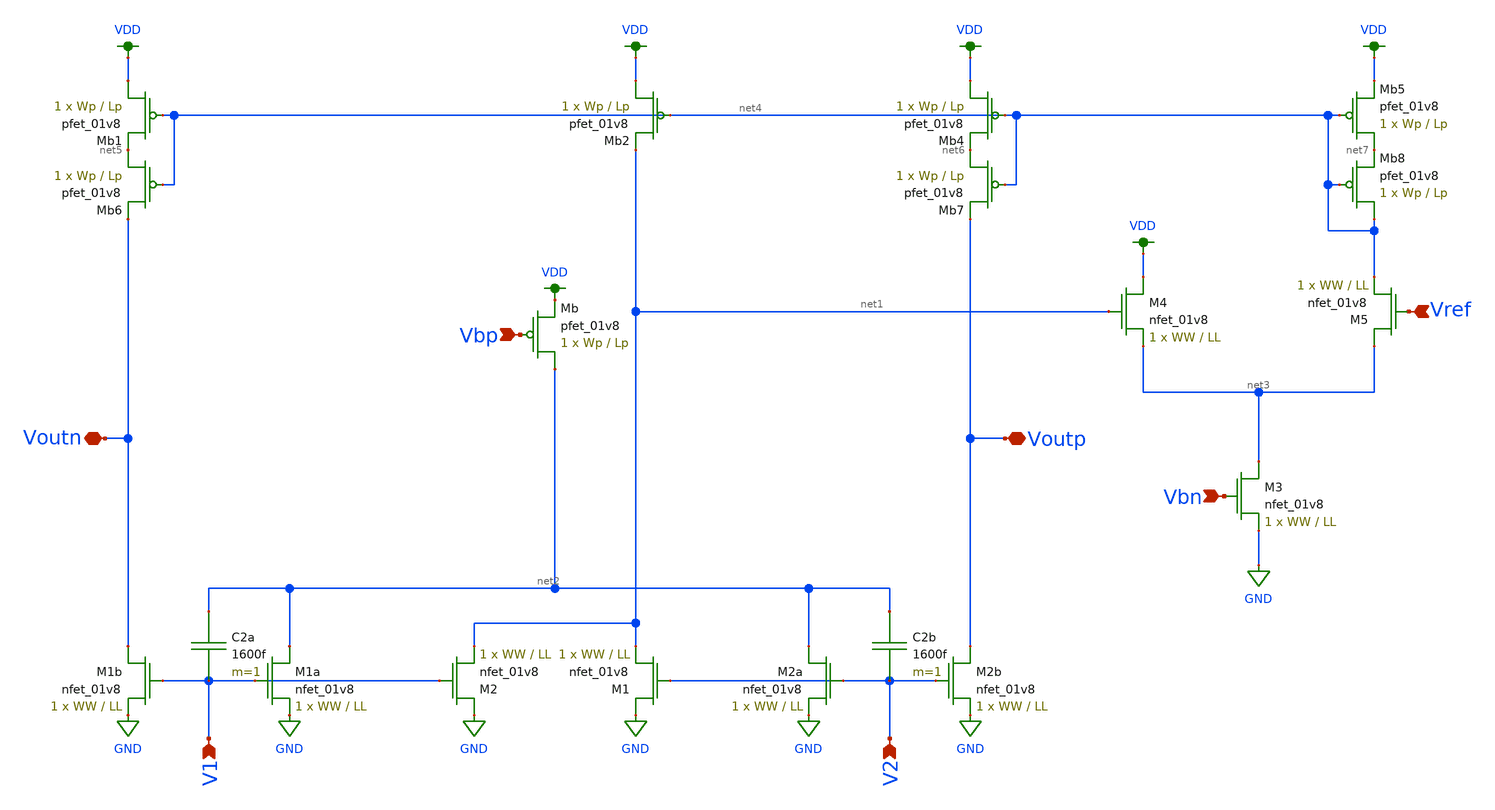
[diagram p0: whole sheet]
** sch_path: schematic/archive/fully_differential_sc_amp.sch
**.subckt fully_differential_sc_amp V1 V2 Vbp Vbn Vref Voutp Voutn
*.ipin V1
*.ipin V2
*.ipin Vbp
*.ipin Vbn
*.ipin Vref
*.iopin Voutp
*.iopin Voutn
XM1a net2 V1 GND GND sky130_fd_pr__nfet_01v8 L=LL W=WW nf=1 ad='int((nf+1)/2) * W/nf * 0.29' as='int((nf+2)/2) * W/nf * 0.29'
+ pd='2*int((nf+1)/2) * (W/nf + 0.29)' ps='2*int((nf+2)/2) * (W/nf + 0.29)' nrd='0.29 / W' nrs='0.29 / W'
+ sa=0 sb=0 sd=0 mult=1 m=1
XM1b Voutn V1 GND GND sky130_fd_pr__nfet_01v8 L=LL W=WW nf=1 ad='int((nf+1)/2) * W/nf * 0.29' as='int((nf+2)/2) * W/nf * 0.29'
+ pd='2*int((nf+1)/2) * (W/nf + 0.29)' ps='2*int((nf+2)/2) * (W/nf + 0.29)' nrd='0.29 / W' nrs='0.29 / W'
+ sa=0 sb=0 sd=0 mult=1 m=1
XM2b Voutp V2 GND GND sky130_fd_pr__nfet_01v8 L=LL W=WW nf=1 ad='int((nf+1)/2) * W/nf * 0.29' as='int((nf+2)/2) * W/nf * 0.29'
+ pd='2*int((nf+1)/2) * (W/nf + 0.29)' ps='2*int((nf+2)/2) * (W/nf + 0.29)' nrd='0.29 / W' nrs='0.29 / W'
+ sa=0 sb=0 sd=0 mult=1 m=1
XM2a net2 V2 GND GND sky130_fd_pr__nfet_01v8 L=LL W=WW nf=1 ad='int((nf+1)/2) * W/nf * 0.29' as='int((nf+2)/2) * W/nf * 0.29'
+ pd='2*int((nf+1)/2) * (W/nf + 0.29)' ps='2*int((nf+2)/2) * (W/nf + 0.29)' nrd='0.29 / W' nrs='0.29 / W'
+ sa=0 sb=0 sd=0 mult=1 m=1
XMb net2 Vbp VDD VDD sky130_fd_pr__pfet_01v8 L=Lp W=Wp nf=1 ad='int((nf+1)/2) * W/nf * 0.29' as='int((nf+2)/2) * W/nf * 0.29'
+ pd='2*int((nf+1)/2) * (W/nf + 0.29)' ps='2*int((nf+2)/2) * (W/nf + 0.29)' nrd='0.29 / W' nrs='0.29 / W'
+ sa=0 sb=0 sd=0 mult=1 m=1
C2b net2 V2 1600f m=1
C2a net2 V1 1600f m=1
XM1 GND V2 net1 GND sky130_fd_pr__nfet_01v8 L=LL W=WW nf=1 ad='int((nf+1)/2) * W/nf * 0.29' as='int((nf+2)/2) * W/nf * 0.29'
+ pd='2*int((nf+1)/2) * (W/nf + 0.29)' ps='2*int((nf+2)/2) * (W/nf + 0.29)' nrd='0.29 / W' nrs='0.29 / W'
+ sa=0 sb=0 sd=0 mult=1 m=1
XM2 GND V1 net1 GND sky130_fd_pr__nfet_01v8 L=LL W=WW nf=1 ad='int((nf+1)/2) * W/nf * 0.29' as='int((nf+2)/2) * W/nf * 0.29'
+ pd='2*int((nf+1)/2) * (W/nf + 0.29)' ps='2*int((nf+2)/2) * (W/nf + 0.29)' nrd='0.29 / W' nrs='0.29 / W'
+ sa=0 sb=0 sd=0 mult=1 m=1
XMb1 VDD net4 net5 VDD sky130_fd_pr__pfet_01v8 L=Lp W=Wp nf=1 ad='int((nf+1)/2) * W/nf * 0.29' as='int((nf+2)/2) * W/nf * 0.29'
+ pd='2*int((nf+1)/2) * (W/nf + 0.29)' ps='2*int((nf+2)/2) * (W/nf + 0.29)' nrd='0.29 / W' nrs='0.29 / W'
+ sa=0 sb=0 sd=0 mult=1 m=1
XMb2 VDD net4 net1 VDD sky130_fd_pr__pfet_01v8 L=Lp W=Wp nf=1 ad='int((nf+1)/2) * W/nf * 0.29' as='int((nf+2)/2) * W/nf * 0.29'
+ pd='2*int((nf+1)/2) * (W/nf + 0.29)' ps='2*int((nf+2)/2) * (W/nf + 0.29)' nrd='0.29 / W' nrs='0.29 / W'
+ sa=0 sb=0 sd=0 mult=1 m=1
XMb4 VDD net4 net6 VDD sky130_fd_pr__pfet_01v8 L=Lp W=Wp nf=1 ad='int((nf+1)/2) * W/nf * 0.29' as='int((nf+2)/2) * W/nf * 0.29'
+ pd='2*int((nf+1)/2) * (W/nf + 0.29)' ps='2*int((nf+2)/2) * (W/nf + 0.29)' nrd='0.29 / W' nrs='0.29 / W'
+ sa=0 sb=0 sd=0 mult=1 m=1
XMb5 net7 net4 VDD VDD sky130_fd_pr__pfet_01v8 L=Lp W=Wp nf=1 ad='int((nf+1)/2) * W/nf * 0.29' as='int((nf+2)/2) * W/nf * 0.29'
+ pd='2*int((nf+1)/2) * (W/nf + 0.29)' ps='2*int((nf+2)/2) * (W/nf + 0.29)' nrd='0.29 / W' nrs='0.29 / W'
+ sa=0 sb=0 sd=0 mult=1 m=1
XM3 net3 Vbn GND GND sky130_fd_pr__nfet_01v8 L=LL W=WW nf=1 ad='int((nf+1)/2) * W/nf * 0.29' as='int((nf+2)/2) * W/nf * 0.29'
+ pd='2*int((nf+1)/2) * (W/nf + 0.29)' ps='2*int((nf+2)/2) * (W/nf + 0.29)' nrd='0.29 / W' nrs='0.29 / W'
+ sa=0 sb=0 sd=0 mult=1 m=1
XM4 VDD net1 net3 GND sky130_fd_pr__nfet_01v8 L=LL W=WW nf=1 ad='int((nf+1)/2) * W/nf * 0.29' as='int((nf+2)/2) * W/nf * 0.29'
+ pd='2*int((nf+1)/2) * (W/nf + 0.29)' ps='2*int((nf+2)/2) * (W/nf + 0.29)' nrd='0.29 / W' nrs='0.29 / W'
+ sa=0 sb=0 sd=0 mult=1 m=1
XM5 net3 Vref net4 GND sky130_fd_pr__nfet_01v8 L=LL W=WW nf=1 ad='int((nf+1)/2) * W/nf * 0.29' as='int((nf+2)/2) * W/nf * 0.29'
+ pd='2*int((nf+1)/2) * (W/nf + 0.29)' ps='2*int((nf+2)/2) * (W/nf + 0.29)' nrd='0.29 / W' nrs='0.29 / W'
+ sa=0 sb=0 sd=0 mult=1 m=1
XMb6 net5 net4 Voutn VDD sky130_fd_pr__pfet_01v8 L=Lp W=Wp nf=1 ad='int((nf+1)/2) * W/nf * 0.29' as='int((nf+2)/2) * W/nf * 0.29'
+ pd='2*int((nf+1)/2) * (W/nf + 0.29)' ps='2*int((nf+2)/2) * (W/nf + 0.29)' nrd='0.29 / W' nrs='0.29 / W'
+ sa=0 sb=0 sd=0 mult=1 m=1
XMb7 net6 net4 Voutp VDD sky130_fd_pr__pfet_01v8 L=Lp W=Wp nf=1 ad='int((nf+1)/2) * W/nf * 0.29' as='int((nf+2)/2) * W/nf * 0.29'
+ pd='2*int((nf+1)/2) * (W/nf + 0.29)' ps='2*int((nf+2)/2) * (W/nf + 0.29)' nrd='0.29 / W' nrs='0.29 / W'
+ sa=0 sb=0 sd=0 mult=1 m=1
XMb8 net4 net4 net7 VDD sky130_fd_pr__pfet_01v8 L=Lp W=Wp nf=1 ad='int((nf+1)/2) * W/nf * 0.29' as='int((nf+2)/2) * W/nf * 0.29'
+ pd='2*int((nf+1)/2) * (W/nf + 0.29)' ps='2*int((nf+2)/2) * (W/nf + 0.29)' nrd='0.29 / W' nrs='0.29 / W'
+ sa=0 sb=0 sd=0 mult=1 m=1
**.ends
.GLOBAL VDD
.GLOBAL GND
.end
